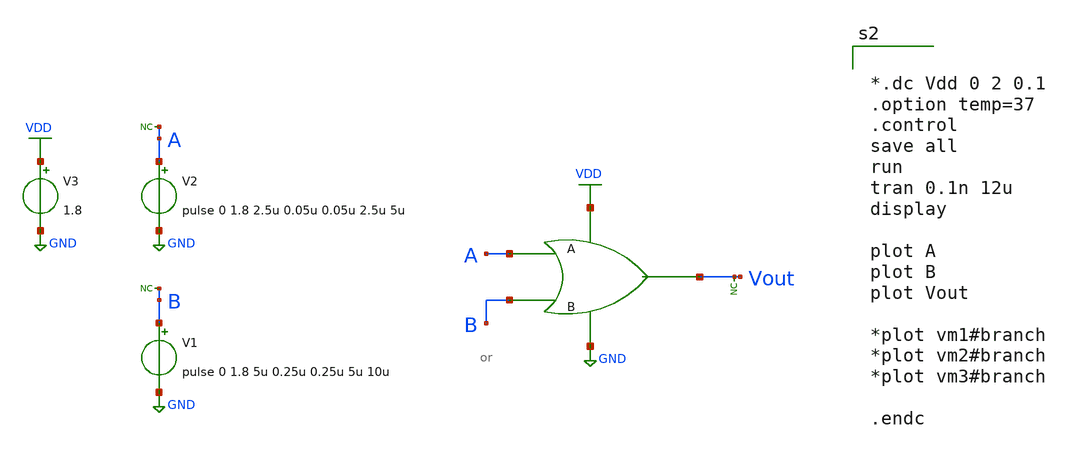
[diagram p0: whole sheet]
** sch_path: xschem/ip_block/logic_gate/tb_or.sch
**.subckt tb_or
V1 B GND pulse 0 1.8 5u 0.25u 0.25u 5u 10u
* noconn B
V2 A GND pulse 0 1.8 2.5u 0.05u 0.05u 2.5u 5u
* noconn A
V3 VDD GND 1.8
X1 A Vout GND VDD B or
* noconn Vout
**** begin user architecture code

** opencircuitdesign pdks install
.lib $::SKYWATER_MODELS/sky130.lib.spice tt




*.dc Vdd 0 2 0.1
.option temp=37
.control
save all
run
tran 0.1n 12u
display

plot A
plot B
plot Vout

*plot vm1#branch
*plot vm2#branch
*plot vm3#branch

.endc


**** end user architecture code
**.ends
.GLOBAL GND
.GLOBAL VDD
.end
